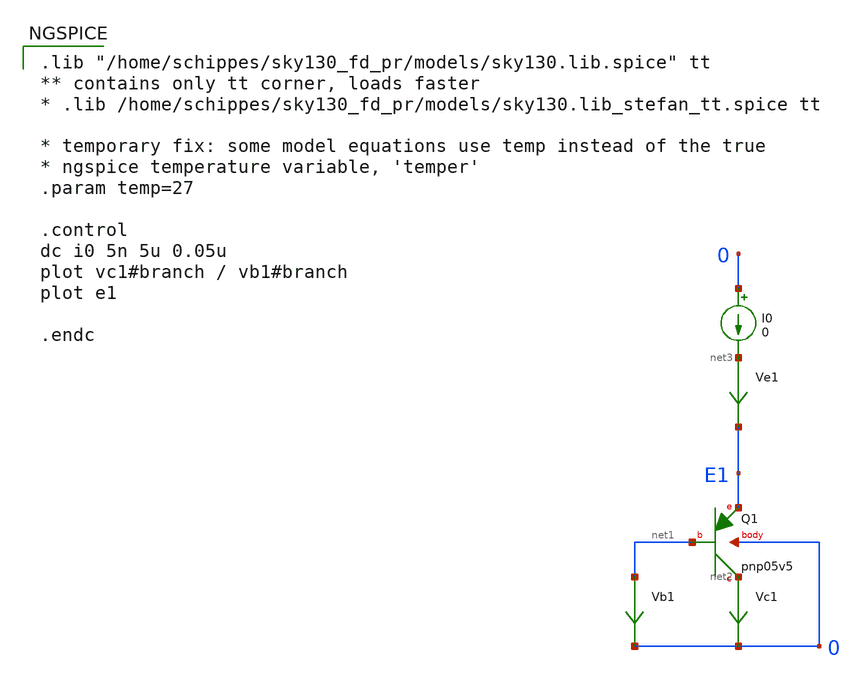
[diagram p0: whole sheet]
** sch_path: sky130_tests/test_bipolar.sch
**.subckt test_bipolar
XQ1 net2 net1 E1 0 sky130_fd_pr__pnp_05v5_W0p68L0p68
Vc1 net2 0 0
.save i(vc1)
Vb1 net1 0 0
.save i(vb1)
I0 0 net3 0
Ve1 net3 E1 0
.save i(ve1)
**** begin user architecture code

.lib "/home/schippes/sky130_fd_pr/models/sky130.lib.spice" tt
** contains only tt corner, loads faster
* .lib /home/schippes/sky130_fd_pr/models/sky130.lib_stefan_tt.spice tt

* temporary fix: some model equations use temp instead of the true
* ngspice temperature variable, 'temper'
.param temp=27

.control
dc i0 5n 5u 0.05u
plot vc1#branch / vb1#branch
plot e1

.endc


**** end user architecture code
**.ends
.end
